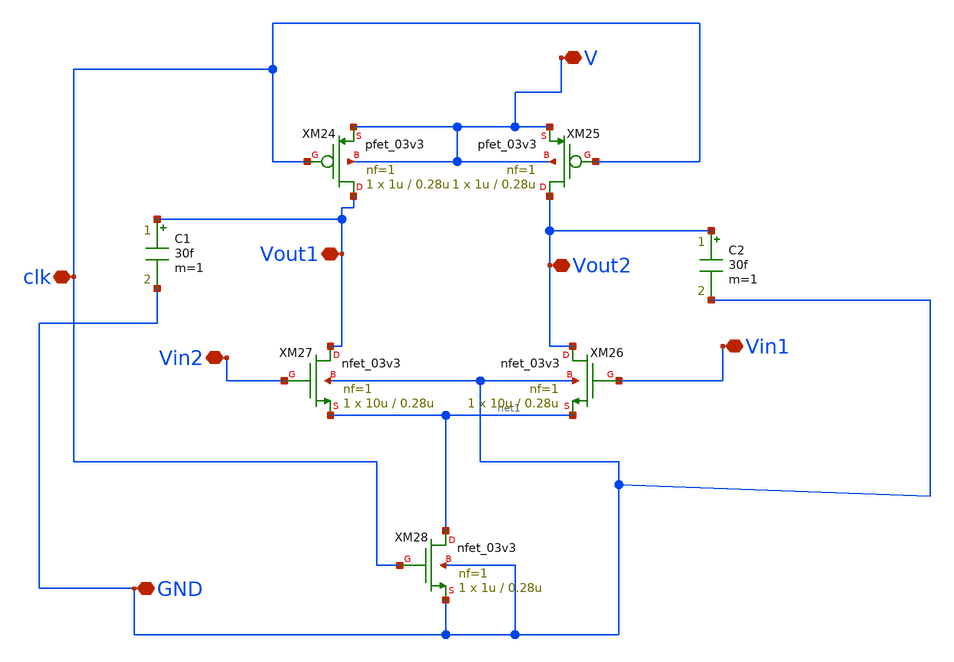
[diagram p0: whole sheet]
** sch_path: Simbolos/preamp.sch
**.subckt preamp V GND Vout2 Vout1 clk Vin2 Vin1
*.iopin V
*.iopin GND
*.iopin Vout2
*.iopin Vout1
*.iopin clk
*.iopin Vin2
*.iopin Vin1
XM26 Vout2 Vin1 net1 GND nfet_03v3 L=0.28u W=10u nf=1 ad='int((nf+1)/2) * W/nf * 0.18u' as='int((nf+2)/2) * W/nf * 0.18u'
+ pd='2*int((nf+1)/2) * (W/nf + 0.18u)' ps='2*int((nf+2)/2) * (W/nf + 0.18u)' nrd='0.18u / W' nrs='0.18u / W'
+ sa=0 sb=0 sd=0 m=1
XM27 Vout1 Vin2 net1 GND nfet_03v3 L=0.28u W=10u nf=1 ad='int((nf+1)/2) * W/nf * 0.18u' as='int((nf+2)/2) * W/nf * 0.18u'
+ pd='2*int((nf+1)/2) * (W/nf + 0.18u)' ps='2*int((nf+2)/2) * (W/nf + 0.18u)' nrd='0.18u / W' nrs='0.18u / W'
+ sa=0 sb=0 sd=0 m=1
XM28 net1 clk GND GND nfet_03v3 L=0.28u W=1u nf=1 ad='int((nf+1)/2) * W/nf * 0.18u' as='int((nf+2)/2) * W/nf * 0.18u'
+ pd='2*int((nf+1)/2) * (W/nf + 0.18u)' ps='2*int((nf+2)/2) * (W/nf + 0.18u)' nrd='0.18u / W' nrs='0.18u / W'
+ sa=0 sb=0 sd=0 m=1
XM24 Vout1 clk V V pfet_03v3 L=0.28u W=1u nf=1 ad='int((nf+1)/2) * W/nf * 0.18u' as='int((nf+2)/2) * W/nf * 0.18u'
+ pd='2*int((nf+1)/2) * (W/nf + 0.18u)' ps='2*int((nf+2)/2) * (W/nf + 0.18u)' nrd='0.18u / W' nrs='0.18u / W'
+ sa=0 sb=0 sd=0 m=1
XM25 Vout2 clk V V pfet_03v3 L=0.28u W=1u nf=1 ad='int((nf+1)/2) * W/nf * 0.18u' as='int((nf+2)/2) * W/nf * 0.18u'
+ pd='2*int((nf+1)/2) * (W/nf + 0.18u)' ps='2*int((nf+2)/2) * (W/nf + 0.18u)' nrd='0.18u / W' nrs='0.18u / W'
+ sa=0 sb=0 sd=0 m=1
C1 Vout1 GND 30f m=1
C2 Vout2 GND 30f m=1
**** begin user architecture code

.include /foss/pdks/gf180mcuC/libs.tech/ngspice/design.ngspice
.lib /foss/pdks/gf180mcuC/libs.tech/ngspice/sm141064.ngspice typical

**** end user architecture code
**.ends
.end
